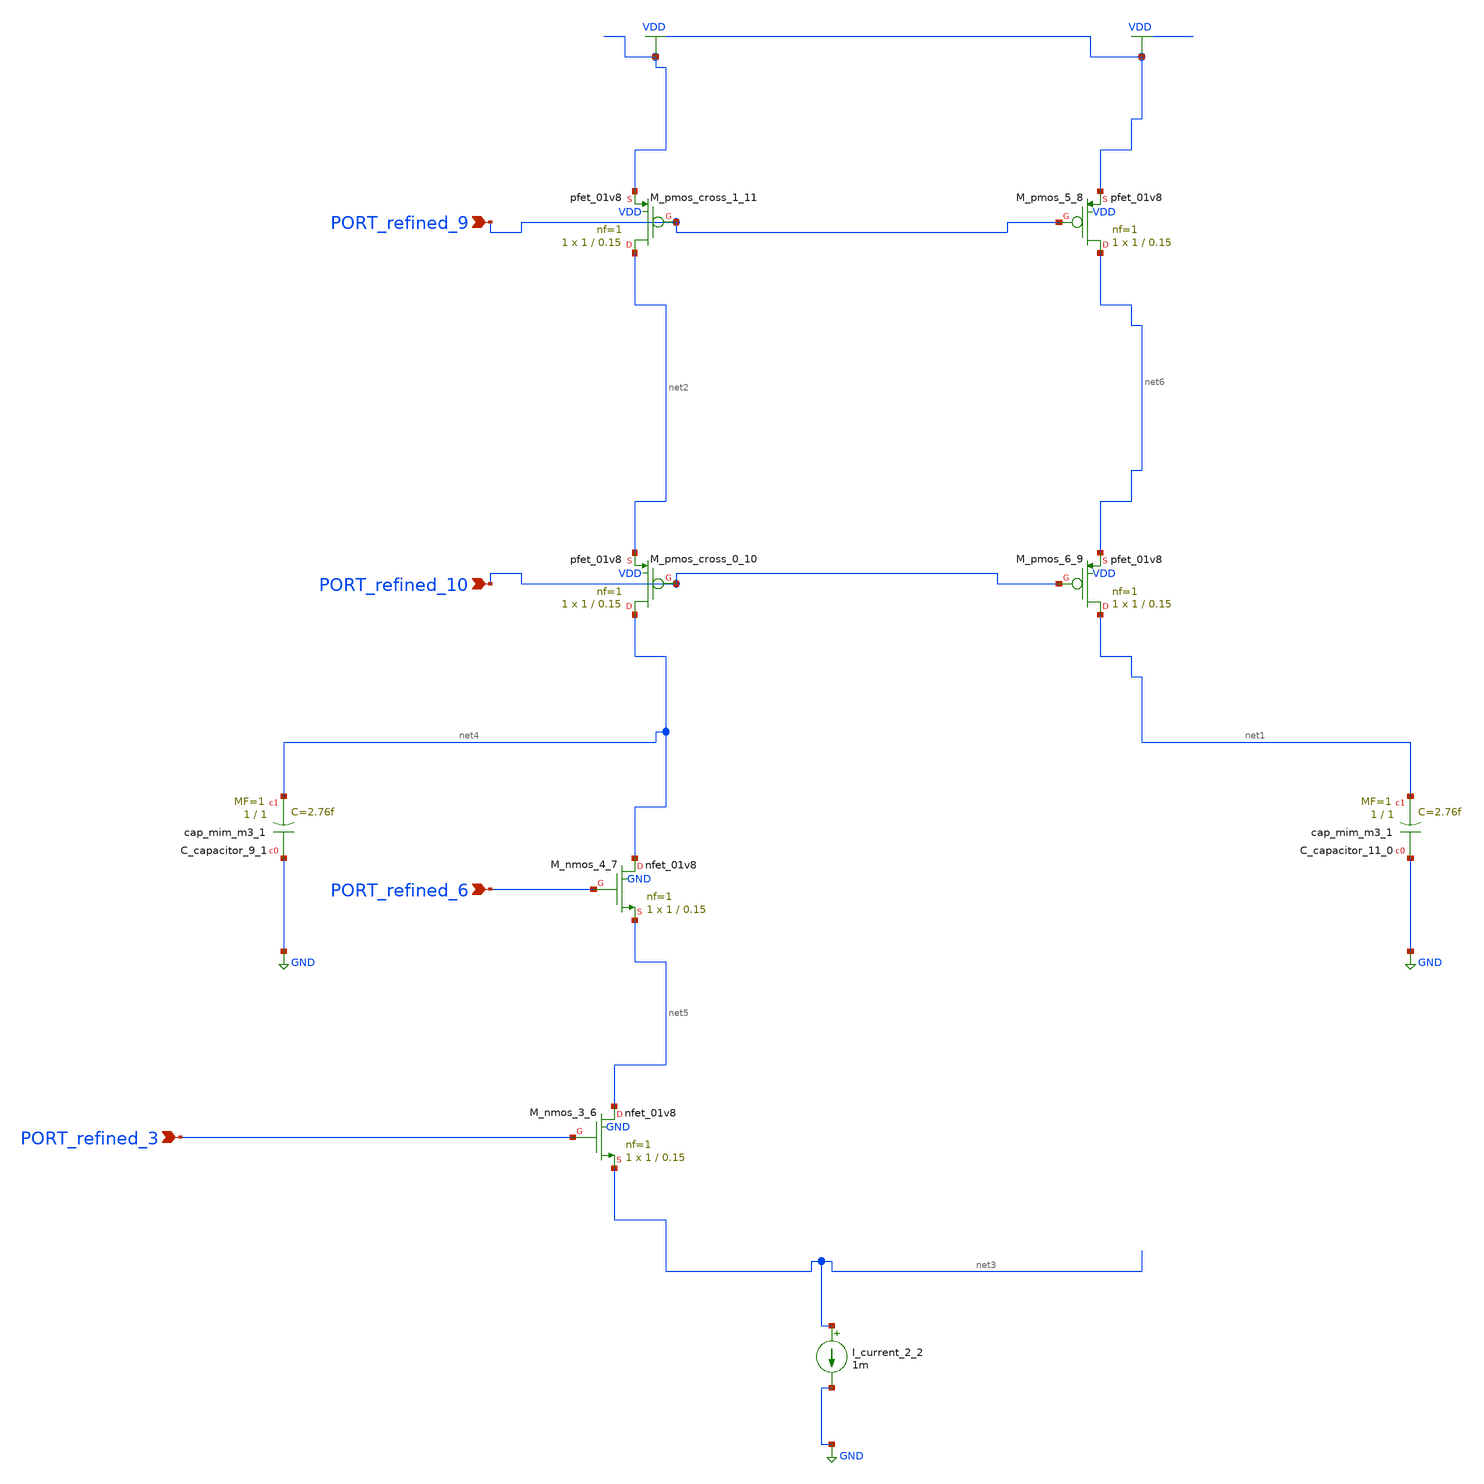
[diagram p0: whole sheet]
** sch_path: schematics/AMSNet/693.sch
**.subckt 693 PORT_refined_3 PORT_refined_10 PORT_refined_9 PORT_refined_6
*.ipin PORT_refined_3
*.ipin PORT_refined_10
*.ipin PORT_refined_9
*.ipin PORT_refined_6
XC_capacitor_11_0 GND net1 sky130_fd_pr__cap_mim_m3_1 W=1 L=1 MF=1 m=1
XC_capacitor_9_1 GND net4 sky130_fd_pr__cap_mim_m3_1 W=1 L=1 MF=1 m=1
I_current_2_2 net3 GND 1m
XM_nmos_3_6 net5 PORT_refined_3 net3 GND sky130_fd_pr__nfet_01v8 L=0.15 W=1 nf=1 ad='int((1 + 1)/2) * 1 / 1 * 0.29'
+ as='int((1 + 2)/2) * 1 / 1 * 0.29' pd='2*int((1 + 1)/2) * (1 / 1 + 0.29)' ps='2*int((1 + 2)/2) * (1 / 1 + 0.29)'
+ nrd='0.29 / 1 ' nrs='0.29 / 1 ' sa=0 sb=0 sd=0 mult=1 m=1
XM_nmos_4_7 net4 PORT_refined_6 net5 GND sky130_fd_pr__nfet_01v8 L=0.15 W=1 nf=1 ad='int((1 + 1)/2) * 1 / 1 * 0.29'
+ as='int((1 + 2)/2) * 1 / 1 * 0.29' pd='2*int((1 + 1)/2) * (1 / 1 + 0.29)' ps='2*int((1 + 2)/2) * (1 / 1 + 0.29)'
+ nrd='0.29 / 1 ' nrs='0.29 / 1 ' sa=0 sb=0 sd=0 mult=1 m=1
XM_pmos_5_8 net6 PORT_refined_9 VDD VDD sky130_fd_pr__pfet_01v8 L=0.15 W=1 nf=1 ad='int((1 + 1)/2) * 1 / 1 * 0.29'
+ as='int((1 + 2)/2) * 1 / 1 * 0.29' pd='2*int((1 + 1)/2) * (1 / 1 + 0.29)' ps='2*int((1 + 2)/2) * (1 / 1 + 0.29)'
+ nrd='0.29 / 1 ' nrs='0.29 / 1 ' sa=0 sb=0 sd=0 mult=1 m=1
XM_pmos_6_9 net1 PORT_refined_10 net6 VDD sky130_fd_pr__pfet_01v8 L=0.15 W=1 nf=1 ad='int((1 + 1)/2) * 1 / 1 * 0.29'
+ as='int((1 + 2)/2) * 1 / 1 * 0.29' pd='2*int((1 + 1)/2) * (1 / 1 + 0.29)' ps='2*int((1 + 2)/2) * (1 / 1 + 0.29)'
+ nrd='0.29 / 1 ' nrs='0.29 / 1 ' sa=0 sb=0 sd=0 mult=1 m=1
XM_pmos_cross_0_10 net4 PORT_refined_10 net2 VDD sky130_fd_pr__pfet_01v8 L=0.15 W=1 nf=1 ad='int((1 + 1)/2) * 1 / 1 * 0.29'
+ as='int((1 + 2)/2) * 1 / 1 * 0.29' pd='2*int((1 + 1)/2) * (1 / 1 + 0.29)' ps='2*int((1 + 2)/2) * (1 / 1 + 0.29)'
+ nrd='0.29 / 1 ' nrs='0.29 / 1 ' sa=0 sb=0 sd=0 mult=1 m=1
XM_pmos_cross_1_11 net2 PORT_refined_9 VDD VDD sky130_fd_pr__pfet_01v8 L=0.15 W=1 nf=1 ad='int((1 + 1)/2) * 1 / 1 * 0.29'
+ as='int((1 + 2)/2) * 1 / 1 * 0.29' pd='2*int((1 + 1)/2) * (1 / 1 + 0.29)' ps='2*int((1 + 2)/2) * (1 / 1 + 0.29)'
+ nrd='0.29 / 1 ' nrs='0.29 / 1 ' sa=0 sb=0 sd=0 mult=1 m=1
**.ends
.GLOBAL GND
.GLOBAL VDD
.end
